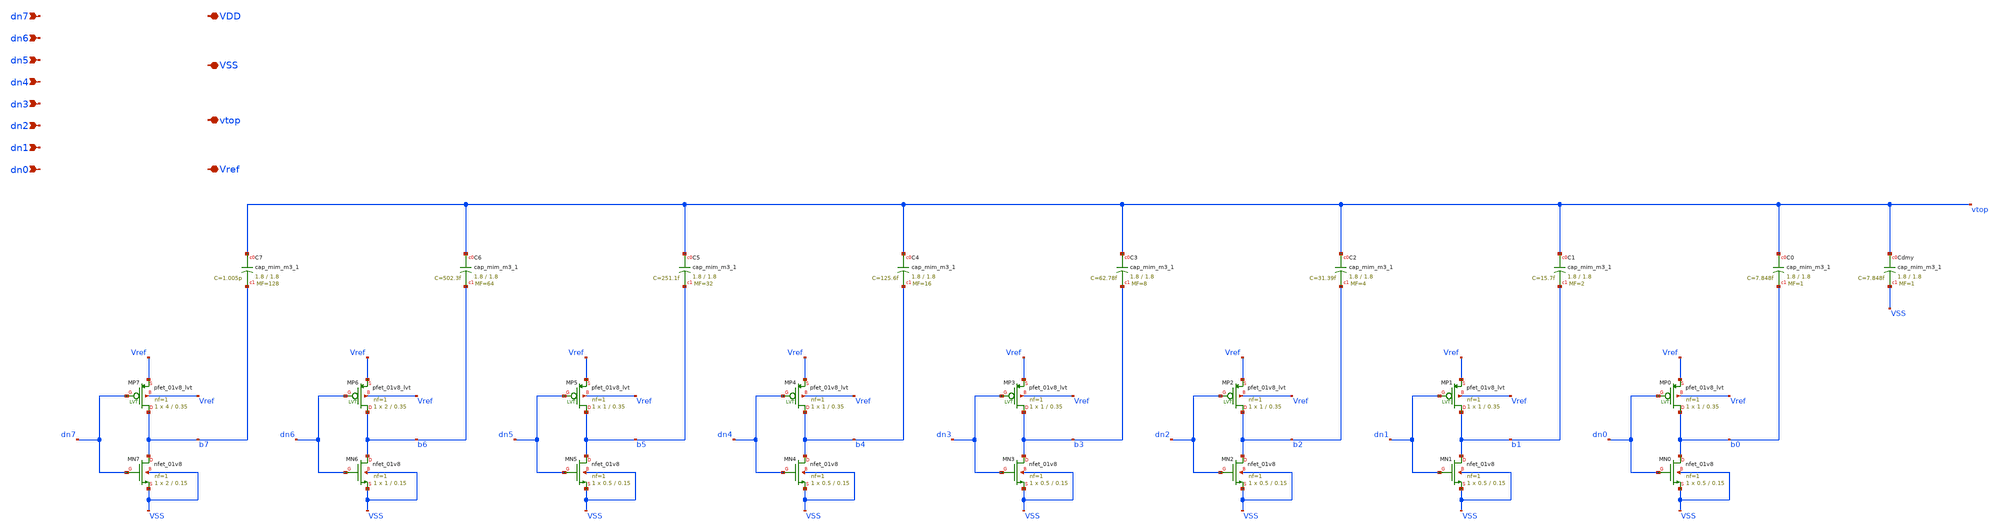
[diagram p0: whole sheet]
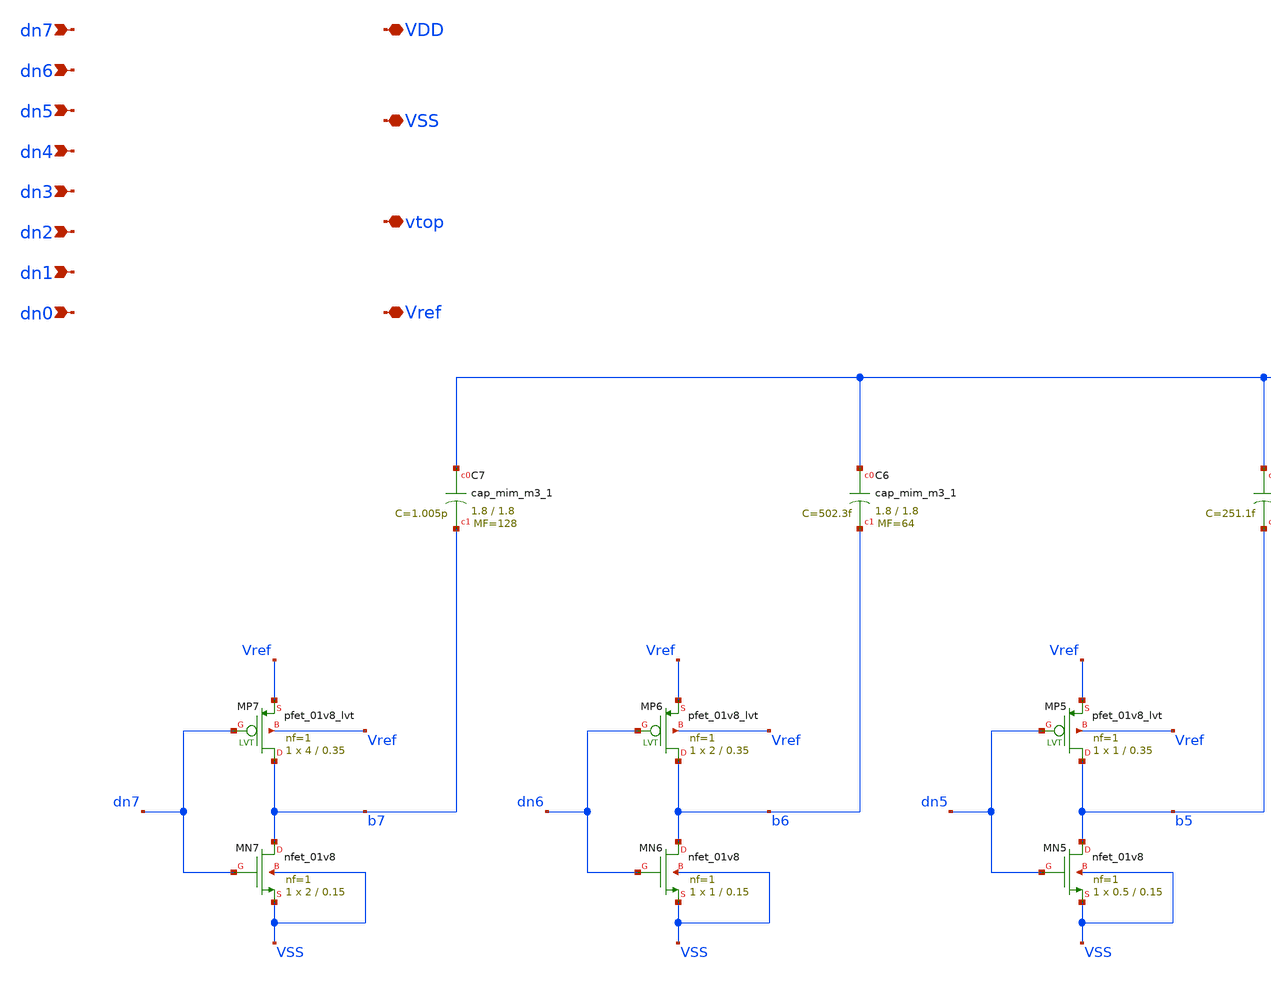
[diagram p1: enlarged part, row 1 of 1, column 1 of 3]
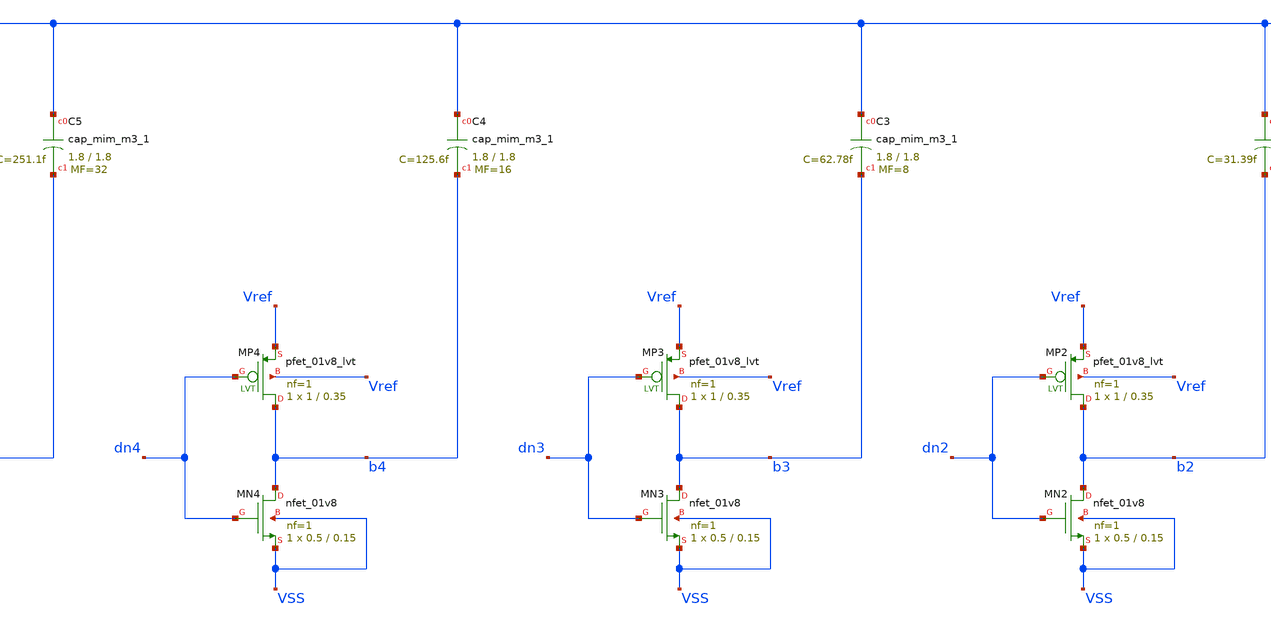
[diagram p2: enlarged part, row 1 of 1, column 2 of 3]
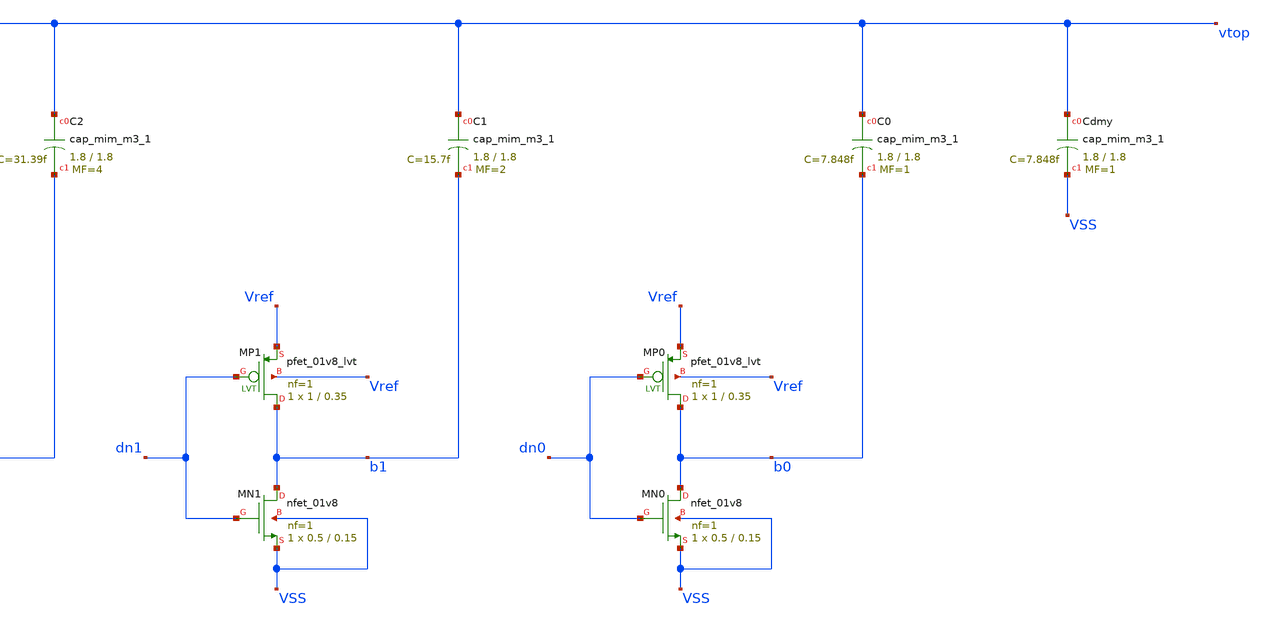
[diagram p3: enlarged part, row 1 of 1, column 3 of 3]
** sch_path: xschem/cdac.sch
**.subckt cdac dn7 dn6 dn5 dn4 dn3 dn2 dn1 dn0 VDD VSS vtop Vref
*.ipin dn7
*.ipin dn6
*.ipin dn5
*.ipin dn4
*.ipin dn3
*.ipin dn2
*.ipin dn1
*.ipin dn0
*.iopin VDD
*.iopin VSS
*.iopin vtop
*.iopin Vref
XMN7 b7 dn7 VSS VSS sky130_fd_pr__nfet_01v8 L=0.15 W=2 nf=1 ad='int((1 + 1)/2) * 2 / 1 * 0.29' as='int((1 + 2)/2) * 2 / 1 * 0.29'
+ pd='2*int((1 + 1)/2) * (2 / 1 + 0.29)' ps='2*int((1 + 2)/2) * (2 / 1 + 0.29)' nrd='0.29 / 2 ' nrs='0.29 / 2 '
+ sa=0 sb=0 sd=0 mult=1 m=1
XMP7 b7 dn7 Vref Vref sky130_fd_pr__pfet_01v8_lvt L=0.35 W=4 nf=1 ad='int((1 + 1)/2) * 4 / 1 * 0.29'
+ as='int((1 + 2)/2) * 4 / 1 * 0.29' pd='2*int((1 + 1)/2) * (4 / 1 + 0.29)' ps='2*int((1 + 2)/2) * (4 / 1 + 0.29)'
+ nrd='0.29 / 4 ' nrs='0.29 / 4 ' sa=0 sb=0 sd=0 mult=1 m=1
XC7 vtop b7 sky130_fd_pr__cap_mim_m3_1 W=1.8 L=1.8 MF=128 m=128
XMN6 b6 dn6 VSS VSS sky130_fd_pr__nfet_01v8 L=0.15 W=1 nf=1 ad='int((1 + 1)/2) * 1 / 1 * 0.29' as='int((1 + 2)/2) * 1 / 1 * 0.29'
+ pd='2*int((1 + 1)/2) * (1 / 1 + 0.29)' ps='2*int((1 + 2)/2) * (1 / 1 + 0.29)' nrd='0.29 / 1 ' nrs='0.29 / 1 '
+ sa=0 sb=0 sd=0 mult=1 m=1
XMP6 b6 dn6 Vref Vref sky130_fd_pr__pfet_01v8_lvt L=0.35 W=2 nf=1 ad='int((1 + 1)/2) * 2 / 1 * 0.29'
+ as='int((1 + 2)/2) * 2 / 1 * 0.29' pd='2*int((1 + 1)/2) * (2 / 1 + 0.29)' ps='2*int((1 + 2)/2) * (2 / 1 + 0.29)'
+ nrd='0.29 / 2 ' nrs='0.29 / 2 ' sa=0 sb=0 sd=0 mult=1 m=1
XC6 vtop b6 sky130_fd_pr__cap_mim_m3_1 W=1.8 L=1.8 MF=64 m=64
XMN5 b5 dn5 VSS VSS sky130_fd_pr__nfet_01v8 L=0.15 W=0.5 nf=1 ad='int((1 + 1)/2) * 0.5 / 1 * 0.29' as='int((1 + 2)/2) * 0.5 / 1 * 0.29'
+ pd='2*int((1 + 1)/2) * (0.5 / 1 + 0.29)' ps='2*int((1 + 2)/2) * (0.5 / 1 + 0.29)' nrd='0.29 / 0.5 ' nrs='0.29 / 0.5 '
+ sa=0 sb=0 sd=0 mult=1 m=1
XMP5 b5 dn5 Vref Vref sky130_fd_pr__pfet_01v8_lvt L=0.35 W=1 nf=1 ad='int((1 + 1)/2) * 1 / 1 * 0.29'
+ as='int((1 + 2)/2) * 1 / 1 * 0.29' pd='2*int((1 + 1)/2) * (1 / 1 + 0.29)' ps='2*int((1 + 2)/2) * (1 / 1 + 0.29)'
+ nrd='0.29 / 1 ' nrs='0.29 / 1 ' sa=0 sb=0 sd=0 mult=1 m=1
XC5 vtop b5 sky130_fd_pr__cap_mim_m3_1 W=1.8 L=1.8 MF=32 m=32
XMN4 b4 dn4 VSS VSS sky130_fd_pr__nfet_01v8 L=0.15 W=0.5 nf=1 ad='int((1 + 1)/2) * 0.5 / 1 * 0.29' as='int((1 + 2)/2) * 0.5 / 1 * 0.29'
+ pd='2*int((1 + 1)/2) * (0.5 / 1 + 0.29)' ps='2*int((1 + 2)/2) * (0.5 / 1 + 0.29)' nrd='0.29 / 0.5 ' nrs='0.29 / 0.5 '
+ sa=0 sb=0 sd=0 mult=1 m=1
XMP4 b4 dn4 Vref Vref sky130_fd_pr__pfet_01v8_lvt L=0.35 W=1 nf=1 ad='int((1 + 1)/2) * 1 / 1 * 0.29'
+ as='int((1 + 2)/2) * 1 / 1 * 0.29' pd='2*int((1 + 1)/2) * (1 / 1 + 0.29)' ps='2*int((1 + 2)/2) * (1 / 1 + 0.29)'
+ nrd='0.29 / 1 ' nrs='0.29 / 1 ' sa=0 sb=0 sd=0 mult=1 m=1
XC4 vtop b4 sky130_fd_pr__cap_mim_m3_1 W=1.8 L=1.8 MF=16 m=16
XMN3 b3 dn3 VSS VSS sky130_fd_pr__nfet_01v8 L=0.15 W=0.5 nf=1 ad='int((1 + 1)/2) * 0.5 / 1 * 0.29' as='int((1 + 2)/2) * 0.5 / 1 * 0.29'
+ pd='2*int((1 + 1)/2) * (0.5 / 1 + 0.29)' ps='2*int((1 + 2)/2) * (0.5 / 1 + 0.29)' nrd='0.29 / 0.5 ' nrs='0.29 / 0.5 '
+ sa=0 sb=0 sd=0 mult=1 m=1
XMP3 b3 dn3 Vref Vref sky130_fd_pr__pfet_01v8_lvt L=0.35 W=1 nf=1 ad='int((1 + 1)/2) * 1 / 1 * 0.29'
+ as='int((1 + 2)/2) * 1 / 1 * 0.29' pd='2*int((1 + 1)/2) * (1 / 1 + 0.29)' ps='2*int((1 + 2)/2) * (1 / 1 + 0.29)'
+ nrd='0.29 / 1 ' nrs='0.29 / 1 ' sa=0 sb=0 sd=0 mult=1 m=1
XC3 vtop b3 sky130_fd_pr__cap_mim_m3_1 W=1.8 L=1.8 MF=8 m=8
XMN2 b2 dn2 VSS VSS sky130_fd_pr__nfet_01v8 L=0.15 W=0.5 nf=1 ad='int((1 + 1)/2) * 0.5 / 1 * 0.29' as='int((1 + 2)/2) * 0.5 / 1 * 0.29'
+ pd='2*int((1 + 1)/2) * (0.5 / 1 + 0.29)' ps='2*int((1 + 2)/2) * (0.5 / 1 + 0.29)' nrd='0.29 / 0.5 ' nrs='0.29 / 0.5 '
+ sa=0 sb=0 sd=0 mult=1 m=1
XMP2 b2 dn2 Vref Vref sky130_fd_pr__pfet_01v8_lvt L=0.35 W=1 nf=1 ad='int((1 + 1)/2) * 1 / 1 * 0.29'
+ as='int((1 + 2)/2) * 1 / 1 * 0.29' pd='2*int((1 + 1)/2) * (1 / 1 + 0.29)' ps='2*int((1 + 2)/2) * (1 / 1 + 0.29)'
+ nrd='0.29 / 1 ' nrs='0.29 / 1 ' sa=0 sb=0 sd=0 mult=1 m=1
XC2 vtop b2 sky130_fd_pr__cap_mim_m3_1 W=1.8 L=1.8 MF=4 m=4
XMN1 b1 dn1 VSS VSS sky130_fd_pr__nfet_01v8 L=0.15 W=0.5 nf=1 ad='int((1 + 1)/2) * 0.5 / 1 * 0.29' as='int((1 + 2)/2) * 0.5 / 1 * 0.29'
+ pd='2*int((1 + 1)/2) * (0.5 / 1 + 0.29)' ps='2*int((1 + 2)/2) * (0.5 / 1 + 0.29)' nrd='0.29 / 0.5 ' nrs='0.29 / 0.5 '
+ sa=0 sb=0 sd=0 mult=1 m=1
XMP1 b1 dn1 Vref Vref sky130_fd_pr__pfet_01v8_lvt L=0.35 W=1 nf=1 ad='int((1 + 1)/2) * 1 / 1 * 0.29'
+ as='int((1 + 2)/2) * 1 / 1 * 0.29' pd='2*int((1 + 1)/2) * (1 / 1 + 0.29)' ps='2*int((1 + 2)/2) * (1 / 1 + 0.29)'
+ nrd='0.29 / 1 ' nrs='0.29 / 1 ' sa=0 sb=0 sd=0 mult=1 m=1
XC1 vtop b1 sky130_fd_pr__cap_mim_m3_1 W=1.8 L=1.8 MF=2 m=2
XMN0 b0 dn0 VSS VSS sky130_fd_pr__nfet_01v8 L=0.15 W=0.5 nf=1 ad='int((1 + 1)/2) * 0.5 / 1 * 0.29' as='int((1 + 2)/2) * 0.5 / 1 * 0.29'
+ pd='2*int((1 + 1)/2) * (0.5 / 1 + 0.29)' ps='2*int((1 + 2)/2) * (0.5 / 1 + 0.29)' nrd='0.29 / 0.5 ' nrs='0.29 / 0.5 '
+ sa=0 sb=0 sd=0 mult=1 m=1
XMP0 b0 dn0 Vref Vref sky130_fd_pr__pfet_01v8_lvt L=0.35 W=1 nf=1 ad='int((1 + 1)/2) * 1 / 1 * 0.29'
+ as='int((1 + 2)/2) * 1 / 1 * 0.29' pd='2*int((1 + 1)/2) * (1 / 1 + 0.29)' ps='2*int((1 + 2)/2) * (1 / 1 + 0.29)'
+ nrd='0.29 / 1 ' nrs='0.29 / 1 ' sa=0 sb=0 sd=0 mult=1 m=1
XC0 vtop b0 sky130_fd_pr__cap_mim_m3_1 W=1.8 L=1.8 MF=1 m=1
XCdmy vtop VSS sky130_fd_pr__cap_mim_m3_1 W=1.8 L=1.8 MF=1 m=1
**.ends
.end
